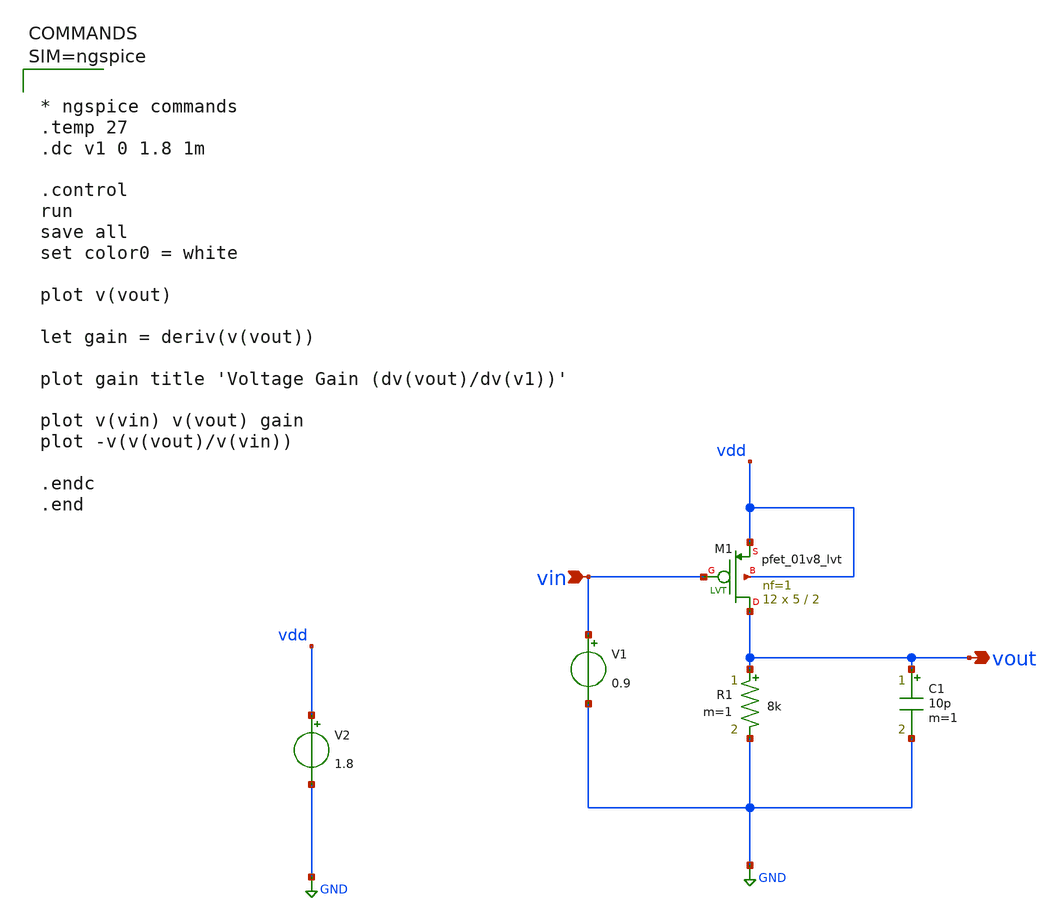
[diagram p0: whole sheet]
** sch_path: sch/PMOS_resLoad_DC_Sweep.sch
**.subckt PMOS_resLoad_DC_Sweep vin vout
*.ipin vin
*.opin vout
XM1 vout vin vdd vdd sky130_fd_pr__pfet_01v8_lvt L=2 W=5 nf=1 ad='int((1 + 1)/2) * 5 / 1 * 0.29' as='int((1 + 2)/2) * 5 / 1 * 0.29'
+ pd='2*int((1 + 1)/2) * (5 / 1 + 0.29)' ps='2*int((1 + 2)/2) * (5 / 1 + 0.29)' nrd='0.29 / 5 ' nrs='0.29 / 5 '
+ sa=0 sb=0 sd=0 mult=12 m=12
R1 vout GND 8k m=1
V1 vin GND 0.9
C1 vout GND 10p m=1
V2 vdd GND 1.8
**** begin user architecture code



* ngspice commands
.temp 27
.dc v1 0 1.8 1m

.control
run
save all
set color0 = white

plot v(vout)

let gain = deriv(v(vout))

plot gain title 'Voltage Gain (dv(vout)/dv(v1))'

plot v(vin) v(vout) gain
plot -v(v(vout)/v(vin))

.endc
.end




** opencircuitdesign pdks install
.lib $::SKYWATER_MODELS/sky130.lib.spice tt

**** end user architecture code
**.ends
.GLOBAL GND
.end
